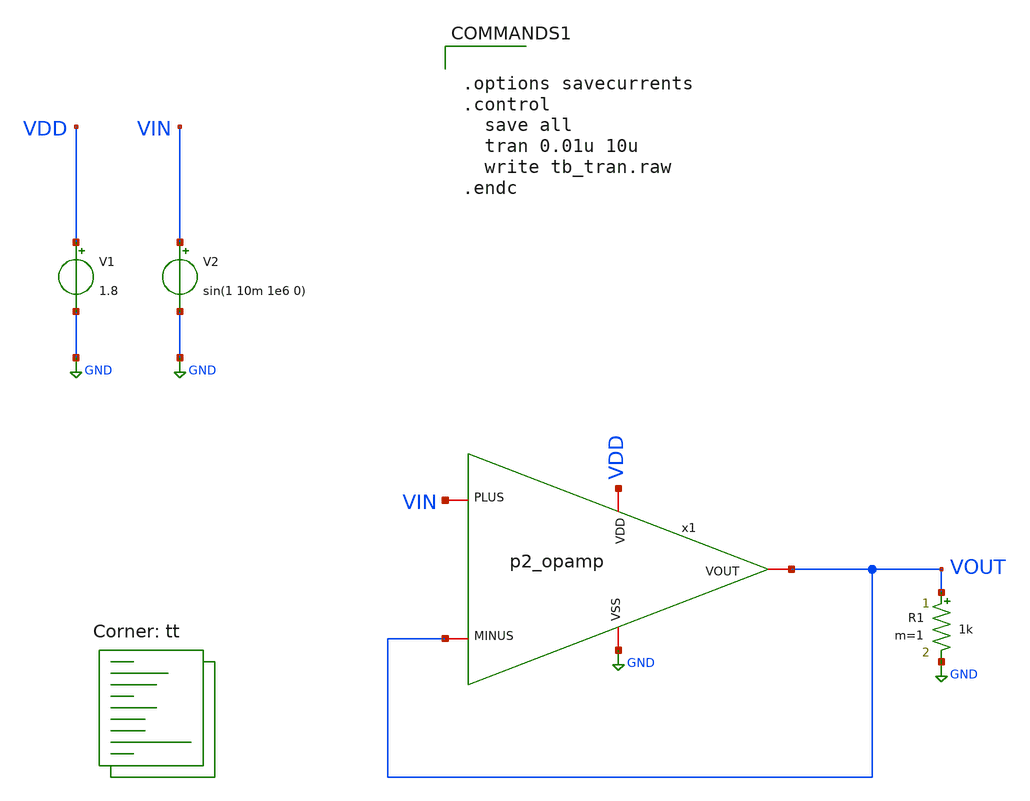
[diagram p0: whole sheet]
** sch_path: xschem/tb_tran.sch
**.subckt tb_tran
x1 VDD VOUT VIN VOUT GND p2_opamp
V1 VDD GND 1.8
R1 VOUT GND 1k m=1
V2 VIN GND sin(1 10m 1e6 0)
**** begin user architecture code
.lib $::SKYWATER_MODELS/sky130.lib.spice tt


.options savecurrents
.control
  save all
  tran 0.01u 10u
  write tb_tran.raw
.endc


**** end user architecture code
**.ends

* expanding   symbol:  p2_opamp.sym # of pins=5
** sym_path: xschem/p2_opamp.sym
** sch_path: xschem/p2_opamp.sch
.subckt p2_opamp VDD MINUS PLUS VOUT VSS
*.iopin VDD
*.iopin VSS
*.iopin PLUS
*.iopin MINUS
*.iopin VOUT
XM2 net2 MINUS net1 VSS sky130_fd_pr__nfet_01v8 L=0.15 W=16 nf=1 ad='int((nf+1)/2) * W/nf * 0.29' as='int((nf+2)/2) * W/nf * 0.29'
+ pd='2*int((nf+1)/2) * (W/nf + 0.29)' ps='2*int((nf+2)/2) * (W/nf + 0.29)' nrd='0.29 / W' nrs='0.29 / W'
+ sa=0 sb=0 sd=0 mult=1 m=1
XM1 net4 PLUS net1 VSS sky130_fd_pr__nfet_01v8 L=0.15 W=16 nf=1 ad='int((nf+1)/2) * W/nf * 0.29' as='int((nf+2)/2) * W/nf * 0.29'
+ pd='2*int((nf+1)/2) * (W/nf + 0.29)' ps='2*int((nf+2)/2) * (W/nf + 0.29)' nrd='0.29 / W' nrs='0.29 / W'
+ sa=0 sb=0 sd=0 mult=1 m=1
XM3 net1 net3 VSS VSS sky130_fd_pr__nfet_01v8 L=0.15 W=4 nf=1 ad='int((nf+1)/2) * W/nf * 0.29' as='int((nf+2)/2) * W/nf * 0.29'
+ pd='2*int((nf+1)/2) * (W/nf + 0.29)' ps='2*int((nf+2)/2) * (W/nf + 0.29)' nrd='0.29 / W' nrs='0.29 / W'
+ sa=0 sb=0 sd=0 mult=1 m=1
XM4 net2 net2 VDD VDD sky130_fd_pr__pfet_01v8 L=0.15 W=32 nf=1 ad='int((nf+1)/2) * W/nf * 0.29' as='int((nf+2)/2) * W/nf * 0.29'
+ pd='2*int((nf+1)/2) * (W/nf + 0.29)' ps='2*int((nf+2)/2) * (W/nf + 0.29)' nrd='0.29 / W' nrs='0.29 / W'
+ sa=0 sb=0 sd=0 mult=1 m=1
XM5 net4 net2 VDD VDD sky130_fd_pr__pfet_01v8 L=0.15 W=32 nf=1 ad='int((nf+1)/2) * W/nf * 0.29' as='int((nf+2)/2) * W/nf * 0.29'
+ pd='2*int((nf+1)/2) * (W/nf + 0.29)' ps='2*int((nf+2)/2) * (W/nf + 0.29)' nrd='0.29 / W' nrs='0.29 / W'
+ sa=0 sb=0 sd=0 mult=1 m=1
XM6 net3 net3 VSS VSS sky130_fd_pr__nfet_01v8 L=0.15 W=1 nf=1 ad='int((nf+1)/2) * W/nf * 0.29' as='int((nf+2)/2) * W/nf * 0.29'
+ pd='2*int((nf+1)/2) * (W/nf + 0.29)' ps='2*int((nf+2)/2) * (W/nf + 0.29)' nrd='0.29 / W' nrs='0.29 / W'
+ sa=0 sb=0 sd=0 mult=1 m=1
XM7 VOUT net3 VSS VSS sky130_fd_pr__nfet_01v8 L=0.15 W=8 nf=1 ad='int((nf+1)/2) * W/nf * 0.29' as='int((nf+2)/2) * W/nf * 0.29'
+ pd='2*int((nf+1)/2) * (W/nf + 0.29)' ps='2*int((nf+2)/2) * (W/nf + 0.29)' nrd='0.29 / W' nrs='0.29 / W'
+ sa=0 sb=0 sd=0 mult=1 m=1
XM8 VOUT net4 VDD VDD sky130_fd_pr__pfet_01v8 L=0.15 W=40 nf=1 ad='int((nf+1)/2) * W/nf * 0.29' as='int((nf+2)/2) * W/nf * 0.29'
+ pd='2*int((nf+1)/2) * (W/nf + 0.29)' ps='2*int((nf+2)/2) * (W/nf + 0.29)' nrd='0.29 / W' nrs='0.29 / W'
+ sa=0 sb=0 sd=0 mult=1 m=1
XC1 VOUT net4 sky130_fd_pr__cap_mim_m3_2 W=1 L=1 MF=1 m=1
XR1 net3 VDD VSS sky130_fd_pr__res_xhigh_po_5p73 L=150 mult=1 m=1
.ends

.GLOBAL GND
.end
